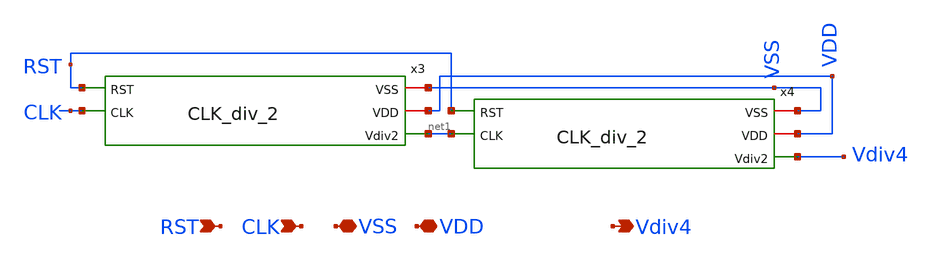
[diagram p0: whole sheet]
** sch_path: Clock_Generator_PAKISTAN_02/Schematics/CLK_div_4.sch
**.subckt CLK_div_4 CLK VSS VDD Vdiv4 RST
*.ipin CLK
*.iopin VSS
*.iopin VDD
*.opin Vdiv4
*.ipin RST
x3 VSS VDD net1 RST CLK CLK_div_2
x4 VSS VDD Vdiv4 RST net1 CLK_div_2
**.ends
.end
